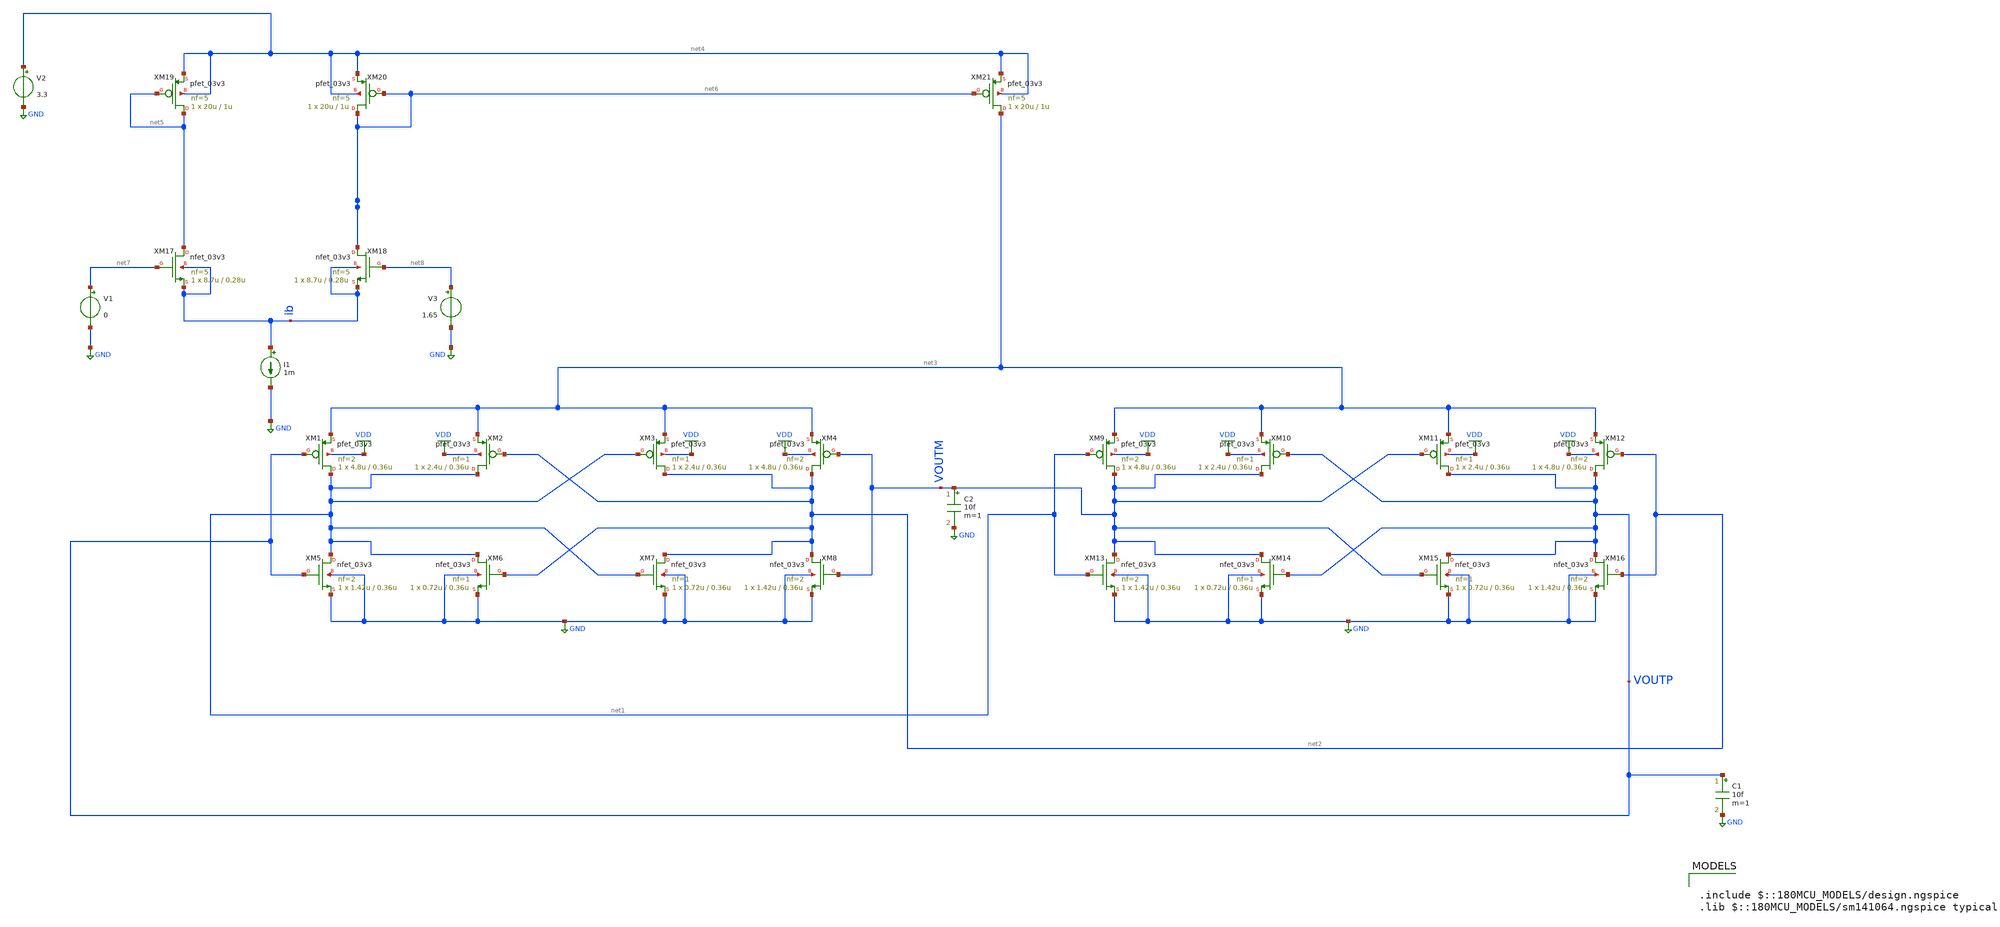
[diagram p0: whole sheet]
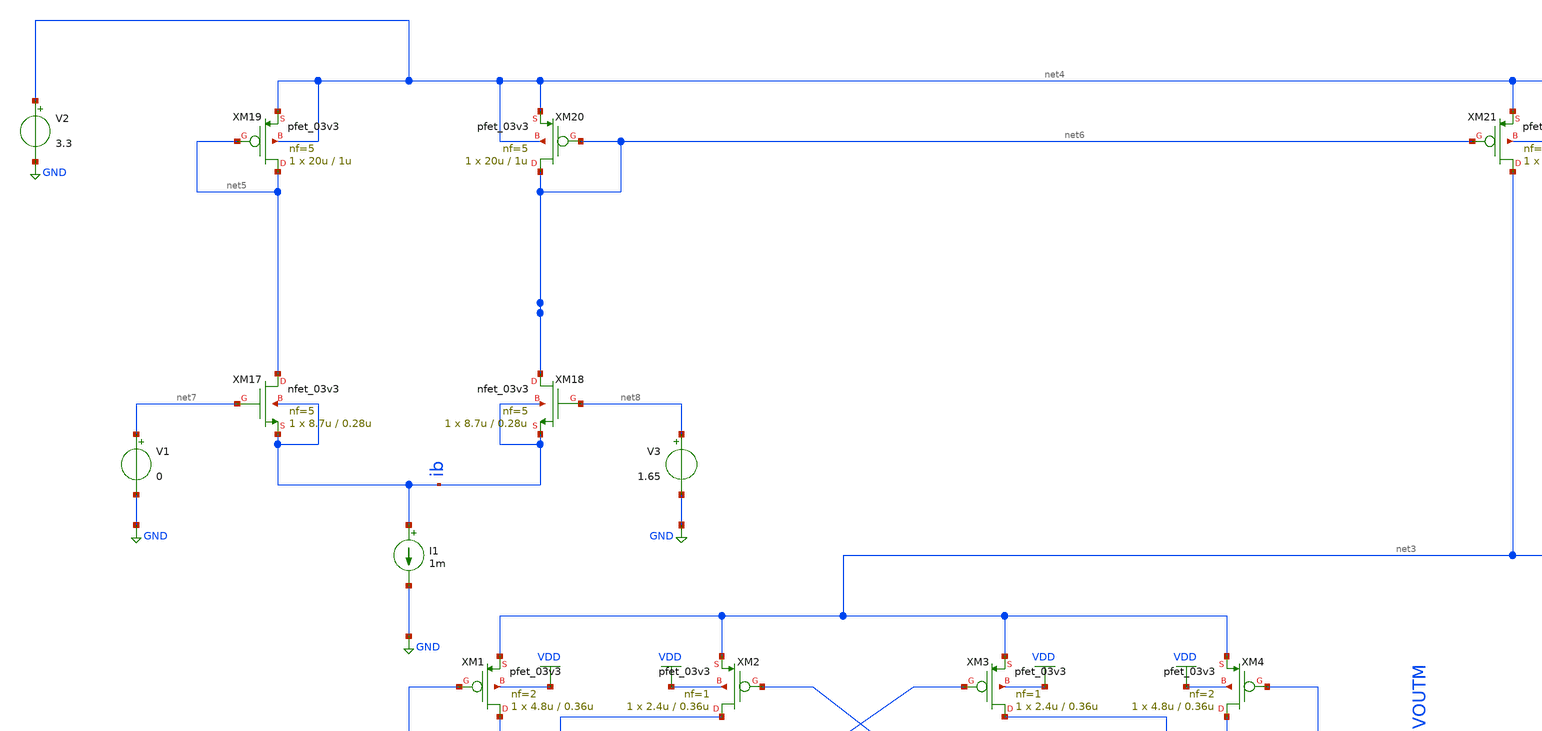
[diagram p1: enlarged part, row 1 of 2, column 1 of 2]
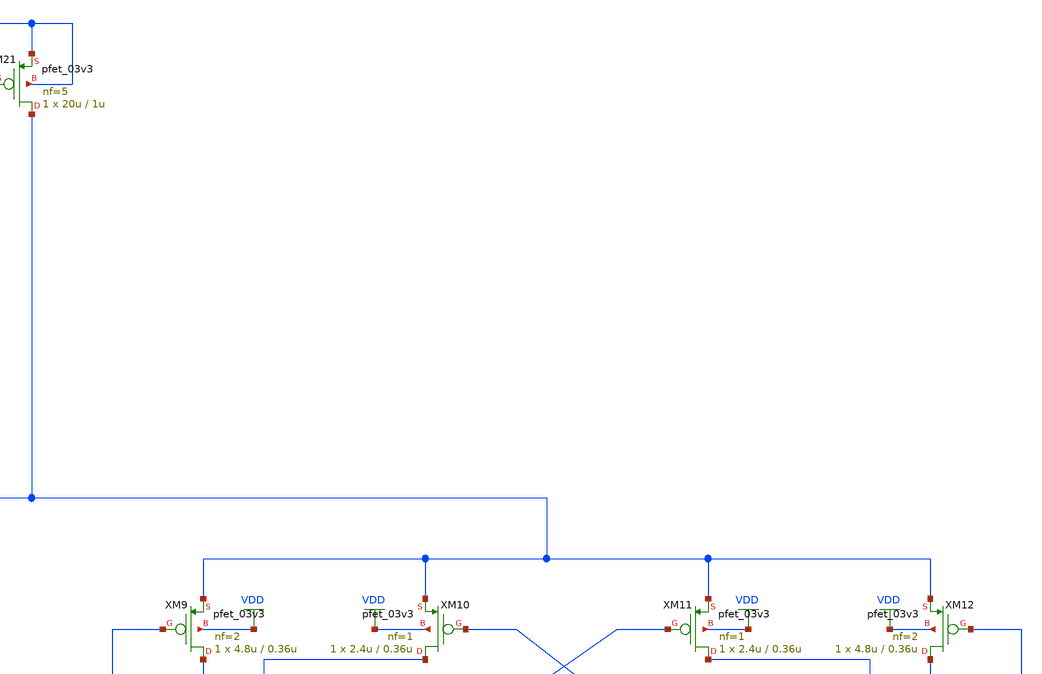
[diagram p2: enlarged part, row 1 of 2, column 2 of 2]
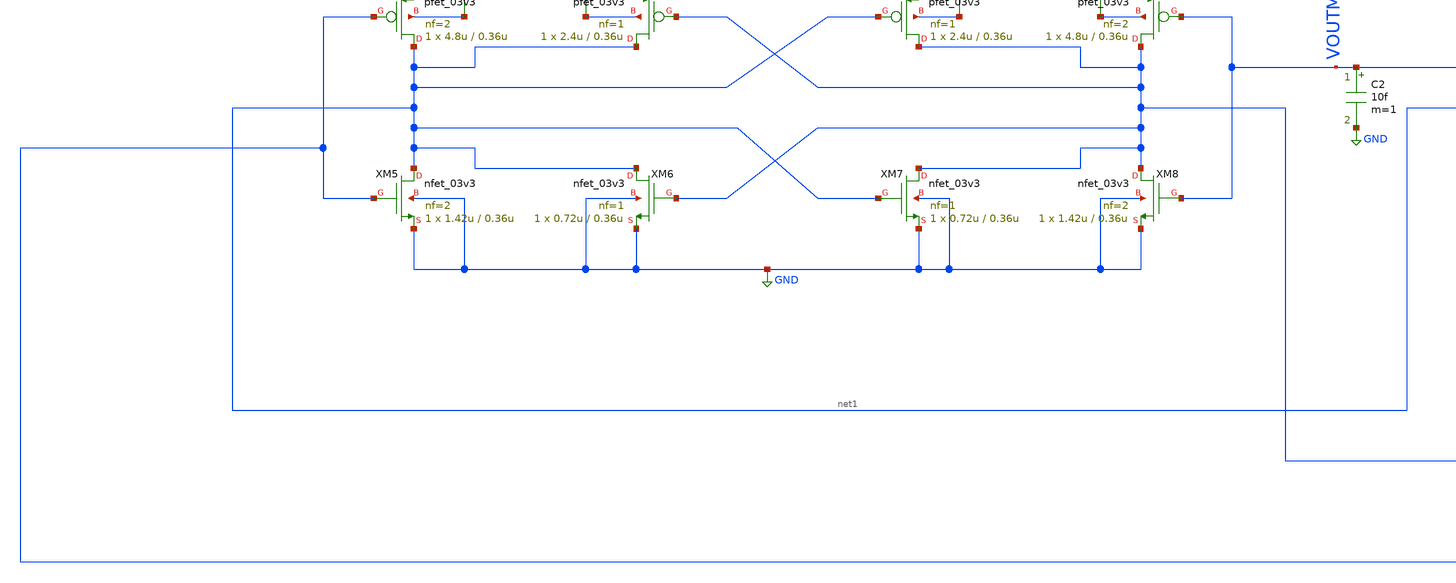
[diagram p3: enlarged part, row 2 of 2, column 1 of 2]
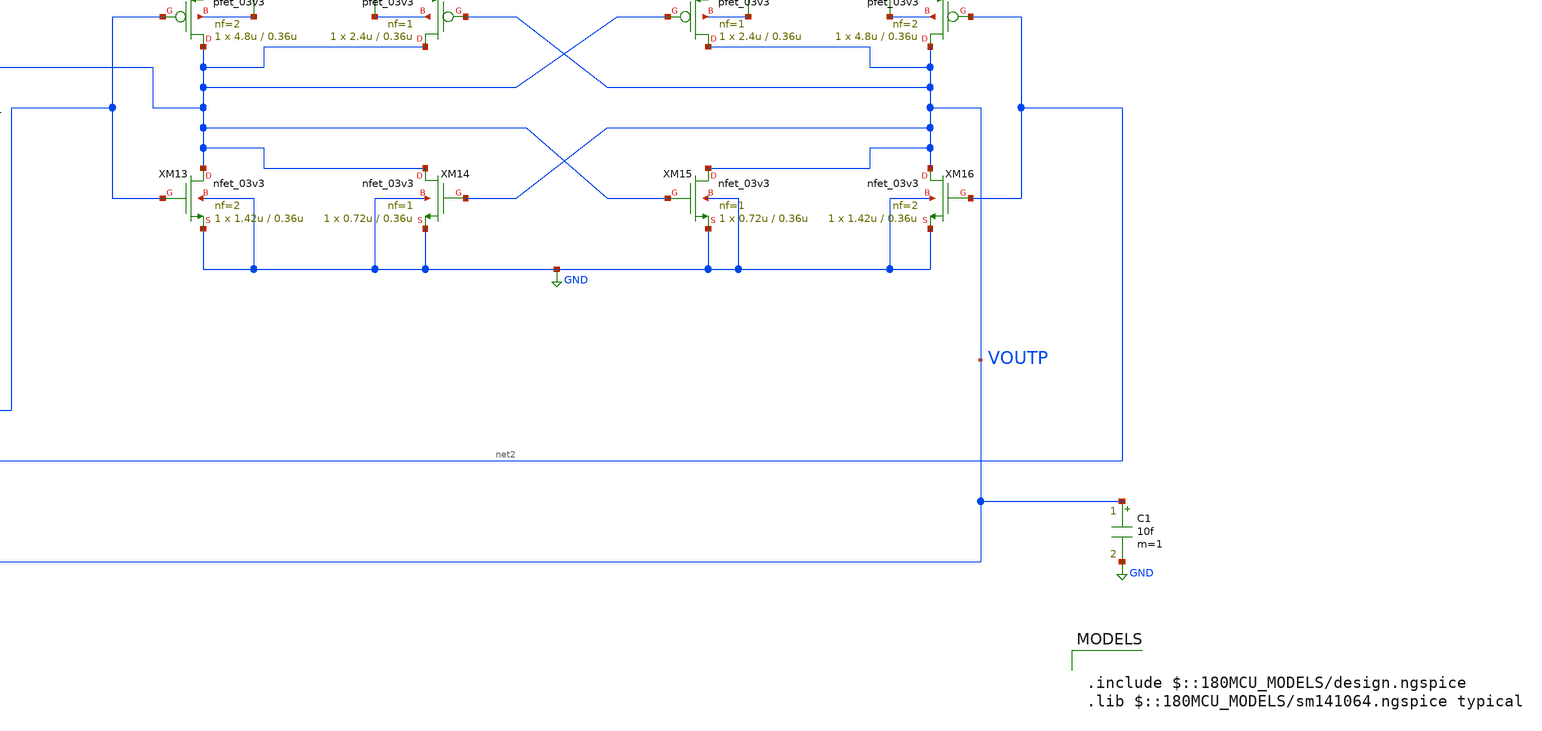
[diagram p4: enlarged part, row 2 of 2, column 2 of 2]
** sch_path: xschem/delay_tb.sch
**.subckt delay_tb
XM1 net1 VOUTP net3 VDD pfet_03v3 L=0.36u W=4.8u nf=2 ad='int((nf+1)/2) * W/nf * 0.18u' as='int((nf+2)/2) * W/nf * 0.18u'
+ pd='2*int((nf+1)/2) * (W/nf + 0.18u)' ps='2*int((nf+2)/2) * (W/nf + 0.18u)' nrd='0.18u / W' nrs='0.18u / W'
+ sa=0 sb=0 sd=0 m=1
XM2 net1 net2 net3 VDD pfet_03v3 L=0.36u W=2.4u nf=1 ad='int((nf+1)/2) * W/nf * 0.18u' as='int((nf+2)/2) * W/nf * 0.18u'
+ pd='2*int((nf+1)/2) * (W/nf + 0.18u)' ps='2*int((nf+2)/2) * (W/nf + 0.18u)' nrd='0.18u / W' nrs='0.18u / W'
+ sa=0 sb=0 sd=0 m=1
XM3 net2 net1 net3 VDD pfet_03v3 L=0.36u W=2.4u nf=1 ad='int((nf+1)/2) * W/nf * 0.18u' as='int((nf+2)/2) * W/nf * 0.18u'
+ pd='2*int((nf+1)/2) * (W/nf + 0.18u)' ps='2*int((nf+2)/2) * (W/nf + 0.18u)' nrd='0.18u / W' nrs='0.18u / W'
+ sa=0 sb=0 sd=0 m=1
XM4 net2 VOUTM net3 VDD pfet_03v3 L=0.36u W=4.8u nf=2 ad='int((nf+1)/2) * W/nf * 0.18u' as='int((nf+2)/2) * W/nf * 0.18u'
+ pd='2*int((nf+1)/2) * (W/nf + 0.18u)' ps='2*int((nf+2)/2) * (W/nf + 0.18u)' nrd='0.18u / W' nrs='0.18u / W'
+ sa=0 sb=0 sd=0 m=1
XM5 net1 VOUTP GND GND nfet_03v3 L=0.36u W=1.42u nf=2 ad='int((nf+1)/2) * W/nf * 0.18u' as='int((nf+2)/2) * W/nf * 0.18u'
+ pd='2*int((nf+1)/2) * (W/nf + 0.18u)' ps='2*int((nf+2)/2) * (W/nf + 0.18u)' nrd='0.18u / W' nrs='0.18u / W'
+ sa=0 sb=0 sd=0 m=1
XM6 net1 net2 GND GND nfet_03v3 L=0.36u W=0.72u nf=1 ad='int((nf+1)/2) * W/nf * 0.18u' as='int((nf+2)/2) * W/nf * 0.18u'
+ pd='2*int((nf+1)/2) * (W/nf + 0.18u)' ps='2*int((nf+2)/2) * (W/nf + 0.18u)' nrd='0.18u / W' nrs='0.18u / W'
+ sa=0 sb=0 sd=0 m=1
XM7 net2 net1 GND GND nfet_03v3 L=0.36u W=0.72u nf=1 ad='int((nf+1)/2) * W/nf * 0.18u' as='int((nf+2)/2) * W/nf * 0.18u'
+ pd='2*int((nf+1)/2) * (W/nf + 0.18u)' ps='2*int((nf+2)/2) * (W/nf + 0.18u)' nrd='0.18u / W' nrs='0.18u / W'
+ sa=0 sb=0 sd=0 m=1
XM8 net2 VOUTM GND GND nfet_03v3 L=0.36u W=1.42u nf=2 ad='int((nf+1)/2) * W/nf * 0.18u' as='int((nf+2)/2) * W/nf * 0.18u'
+ pd='2*int((nf+1)/2) * (W/nf + 0.18u)' ps='2*int((nf+2)/2) * (W/nf + 0.18u)' nrd='0.18u / W' nrs='0.18u / W'
+ sa=0 sb=0 sd=0 m=1
XM9 VOUTM net1 net3 VDD pfet_03v3 L=0.36u W=4.8u nf=2 ad='int((nf+1)/2) * W/nf * 0.18u' as='int((nf+2)/2) * W/nf * 0.18u'
+ pd='2*int((nf+1)/2) * (W/nf + 0.18u)' ps='2*int((nf+2)/2) * (W/nf + 0.18u)' nrd='0.18u / W' nrs='0.18u / W'
+ sa=0 sb=0 sd=0 m=1
XM10 VOUTM VOUTP net3 VDD pfet_03v3 L=0.36u W=2.4u nf=1 ad='int((nf+1)/2) * W/nf * 0.18u' as='int((nf+2)/2) * W/nf * 0.18u'
+ pd='2*int((nf+1)/2) * (W/nf + 0.18u)' ps='2*int((nf+2)/2) * (W/nf + 0.18u)' nrd='0.18u / W' nrs='0.18u / W'
+ sa=0 sb=0 sd=0 m=1
XM11 VOUTP VOUTM net3 VDD pfet_03v3 L=0.36u W=2.4u nf=1 ad='int((nf+1)/2) * W/nf * 0.18u' as='int((nf+2)/2) * W/nf * 0.18u'
+ pd='2*int((nf+1)/2) * (W/nf + 0.18u)' ps='2*int((nf+2)/2) * (W/nf + 0.18u)' nrd='0.18u / W' nrs='0.18u / W'
+ sa=0 sb=0 sd=0 m=1
XM12 VOUTP net2 net3 VDD pfet_03v3 L=0.36u W=4.8u nf=2 ad='int((nf+1)/2) * W/nf * 0.18u' as='int((nf+2)/2) * W/nf * 0.18u'
+ pd='2*int((nf+1)/2) * (W/nf + 0.18u)' ps='2*int((nf+2)/2) * (W/nf + 0.18u)' nrd='0.18u / W' nrs='0.18u / W'
+ sa=0 sb=0 sd=0 m=1
XM13 VOUTM net1 GND GND nfet_03v3 L=0.36u W=1.42u nf=2 ad='int((nf+1)/2) * W/nf * 0.18u' as='int((nf+2)/2) * W/nf * 0.18u'
+ pd='2*int((nf+1)/2) * (W/nf + 0.18u)' ps='2*int((nf+2)/2) * (W/nf + 0.18u)' nrd='0.18u / W' nrs='0.18u / W'
+ sa=0 sb=0 sd=0 m=1
XM14 VOUTM VOUTP GND GND nfet_03v3 L=0.36u W=0.72u nf=1 ad='int((nf+1)/2) * W/nf * 0.18u' as='int((nf+2)/2) * W/nf * 0.18u'
+ pd='2*int((nf+1)/2) * (W/nf + 0.18u)' ps='2*int((nf+2)/2) * (W/nf + 0.18u)' nrd='0.18u / W' nrs='0.18u / W'
+ sa=0 sb=0 sd=0 m=1
XM15 VOUTP VOUTM GND GND nfet_03v3 L=0.36u W=0.72u nf=1 ad='int((nf+1)/2) * W/nf * 0.18u' as='int((nf+2)/2) * W/nf * 0.18u'
+ pd='2*int((nf+1)/2) * (W/nf + 0.18u)' ps='2*int((nf+2)/2) * (W/nf + 0.18u)' nrd='0.18u / W' nrs='0.18u / W'
+ sa=0 sb=0 sd=0 m=1
XM16 VOUTP net2 GND GND nfet_03v3 L=0.36u W=1.42u nf=2 ad='int((nf+1)/2) * W/nf * 0.18u' as='int((nf+2)/2) * W/nf * 0.18u'
+ pd='2*int((nf+1)/2) * (W/nf + 0.18u)' ps='2*int((nf+2)/2) * (W/nf + 0.18u)' nrd='0.18u / W' nrs='0.18u / W'
+ sa=0 sb=0 sd=0 m=1
C1 VOUTP GND 10f m=1
C2 VOUTM GND 10f m=1
V1 net7 GND 0
V2 net4 GND 3.3
I1 ib GND 1m
V3 net8 GND 1.65
XM17 net5 net7 ib ib nfet_03v3 L=0.28u W=8.7u nf=5 ad='int((nf+1)/2) * W/nf * 0.18u' as='int((nf+2)/2) * W/nf * 0.18u'
+ pd='2*int((nf+1)/2) * (W/nf + 0.18u)' ps='2*int((nf+2)/2) * (W/nf + 0.18u)' nrd='0.18u / W' nrs='0.18u / W'
+ sa=0 sb=0 sd=0 m=1
XM18 net6 net8 ib ib nfet_03v3 L=0.28u W=8.7u nf=5 ad='int((nf+1)/2) * W/nf * 0.18u' as='int((nf+2)/2) * W/nf * 0.18u'
+ pd='2*int((nf+1)/2) * (W/nf + 0.18u)' ps='2*int((nf+2)/2) * (W/nf + 0.18u)' nrd='0.18u / W' nrs='0.18u / W'
+ sa=0 sb=0 sd=0 m=1
XM19 net5 net5 net4 net4 pfet_03v3 L=1u W=20u nf=5 ad='int((nf+1)/2) * W/nf * 0.18u' as='int((nf+2)/2) * W/nf * 0.18u'
+ pd='2*int((nf+1)/2) * (W/nf + 0.18u)' ps='2*int((nf+2)/2) * (W/nf + 0.18u)' nrd='0.18u / W' nrs='0.18u / W'
+ sa=0 sb=0 sd=0 m=1
XM20 net6 net6 net4 net4 pfet_03v3 L=1u W=20u nf=5 ad='int((nf+1)/2) * W/nf * 0.18u' as='int((nf+2)/2) * W/nf * 0.18u'
+ pd='2*int((nf+1)/2) * (W/nf + 0.18u)' ps='2*int((nf+2)/2) * (W/nf + 0.18u)' nrd='0.18u / W' nrs='0.18u / W'
+ sa=0 sb=0 sd=0 m=1
XM21 net3 net6 net4 net4 pfet_03v3 L=1u W=20u nf=5 ad='int((nf+1)/2) * W/nf * 0.18u' as='int((nf+2)/2) * W/nf * 0.18u'
+ pd='2*int((nf+1)/2) * (W/nf + 0.18u)' ps='2*int((nf+2)/2) * (W/nf + 0.18u)' nrd='0.18u / W' nrs='0.18u / W'
+ sa=0 sb=0 sd=0 m=1
**** begin user architecture code

.include $::180MCU_MODELS/design.ngspice
.lib $::180MCU_MODELS/sm141064.ngspice typical



.control
tran 10p 10n
save all
plot (v(voutp) - v(voutm))
.endc


**** end user architecture code
**.ends
.GLOBAL GND
.GLOBAL VDD
.end
